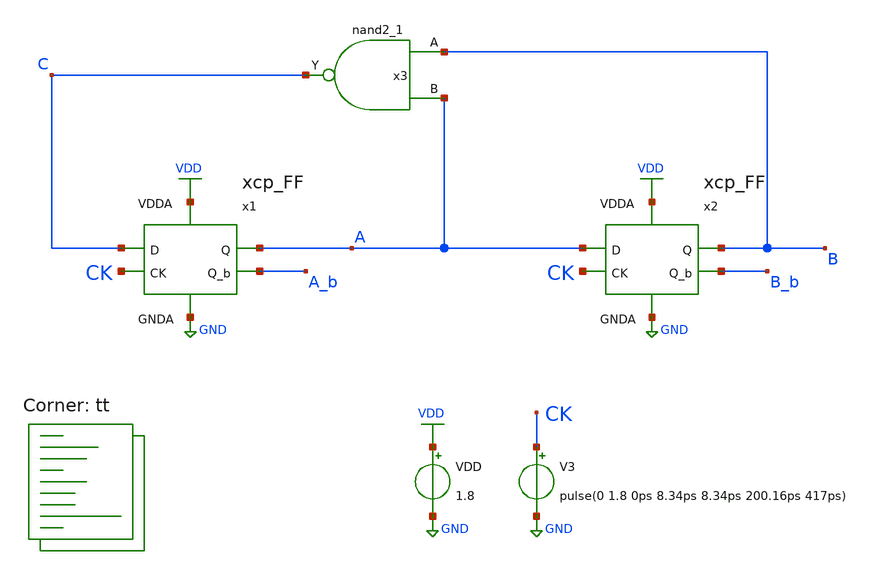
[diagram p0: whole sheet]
** sch_path: projects/pll/divider/xschem_ngspice/tb_xcp_FF_divide3.sch
**.subckt tb_xcp_FF_divide3
VDD VDD GND 1.8
V3 CK GND pulse(0 1.8 0ps 8.34ps 8.34ps 200.16ps 417ps)
x1 VDD C A A_b CK GND xcp_FF
x2 VDD A B B_b CK GND xcp_FF
x3 B A VGND VNB VPB VPWR C sky130_fd_sc_hd__nand2_1
**** begin user architecture code



.include /foss/pdks/sky130A/libs.ref/sky130_fd_sc_hd/spice/sky130_fd_sc_hd.spice

.option method=gear
.option wnflag=1
* .option savecurrents

.save @m.x1.xm1.msky130_fd_pr__nfet_01v8[gm] @m.x1.xm2.msky130_fd_pr__nfet_01v8[gm] @m.x1.xm3.msky130_fd_pr__pfet_01v8[gm] @m.x1.xm4.msky130_fd_pr__pfet_01v8[gm] @m.x1.xm5.msky130_fd_pr__nfet_01v8[gm] @m.x2.xm1.msky130_fd_pr__nfet_01v8[gm] @m.x2.xm2.msky130_fd_pr__nfet_01v8[gm] @m.x2.xm3.msky130_fd_pr__pfet_01v8[gm] @m.x2.xm4.msky130_fd_pr__pfet_01v8[gm] @m.x2.xm5.msky130_fd_pr__nfet_01v8[gm] @v.x1.vmeas @v.x1.vmeas1 @v.x1.vmeas2 @v.x5.vmeas @v.x5.vmeas1 @v.x5.vmeas2


*.ic v(b)=0

.control

  save v(a) v(a_b) v(b) v(b_b) v(c) v(ck)
  * save all
  *tran 0.1n 1u
  tran 0.2p 10n
  *ac dec 20 1 1T
  remzerovec
  write tb_xcp_FF_divide3.raw
  set appendwrite

.endc



.lib $::SKYWATER_MODELS/sky130.lib.spice tt
**** end user architecture code
**.ends

* expanding   symbol:  /foss/designs/my_design/projects/pll/divider/xschem_ngspice/xcp_FF.sym # of
*+ pins=6
** sym_path: projects/pll/divider/xschem_ngspice/xcp_FF.sym
** sch_path: projects/pll/divider/xschem_ngspice/xcp_FF.sch
.subckt xcp_FF VDDA D Q Q_b CK GNDA
*.ipin VDDA
*.opin Q
*.ipin CK
*.ipin GNDA
*.ipin D
*.opin Q_b
x1 VDDA A_b A net2 net3 CK GNDA xcp_latch
x2 VDDA Q_b Q A_b A net1 GNDA xcp_latch
XM1 net1 CK GNDA GNDA sky130_fd_pr__nfet_01v8 L=0.15 W=1 nf=1 ad='int((nf+1)/2) * W/nf * 0.29' as='int((nf+2)/2) * W/nf * 0.29'
+ pd='2*int((nf+1)/2) * (W/nf + 0.29)' ps='2*int((nf+2)/2) * (W/nf + 0.29)' nrd='0.29 / W' nrs='0.29 / W'
+ sa=0 sb=0 sd=0 mult=1 m=1
XM2 net1 CK VDDA VDDA sky130_fd_pr__pfet_01v8 L=0.15 W=1 nf=1 ad='int((nf+1)/2) * W/nf * 0.29' as='int((nf+2)/2) * W/nf * 0.29'
+ pd='2*int((nf+1)/2) * (W/nf + 0.29)' ps='2*int((nf+2)/2) * (W/nf + 0.29)' nrd='0.29 / W' nrs='0.29 / W'
+ sa=0 sb=0 sd=0 mult=1 m=1
XM3 net2 D GNDA GNDA sky130_fd_pr__nfet_01v8 L=0.15 W=1 nf=1 ad='int((nf+1)/2) * W/nf * 0.29' as='int((nf+2)/2) * W/nf * 0.29'
+ pd='2*int((nf+1)/2) * (W/nf + 0.29)' ps='2*int((nf+2)/2) * (W/nf + 0.29)' nrd='0.29 / W' nrs='0.29 / W'
+ sa=0 sb=0 sd=0 mult=1 m=1
XM4 net2 D GNDA GNDA sky130_fd_pr__pfet_01v8 L=0.15 W=1 nf=1 ad='int((nf+1)/2) * W/nf * 0.29' as='int((nf+2)/2) * W/nf * 0.29'
+ pd='2*int((nf+1)/2) * (W/nf + 0.29)' ps='2*int((nf+2)/2) * (W/nf + 0.29)' nrd='0.29 / W' nrs='0.29 / W'
+ sa=0 sb=0 sd=0 mult=1 m=1
XM5 net3 GNDA D VDDA sky130_fd_pr__pfet_01v8 L=0.15 W=1 nf=1 ad='int((nf+1)/2) * W/nf * 0.29' as='int((nf+2)/2) * W/nf * 0.29'
+ pd='2*int((nf+1)/2) * (W/nf + 0.29)' ps='2*int((nf+2)/2) * (W/nf + 0.29)' nrd='0.29 / W' nrs='0.29 / W'
+ sa=0 sb=0 sd=0 mult=1 m=1
XM6 net3 VDDA D GNDA sky130_fd_pr__nfet_01v8 L=0.15 W=1 nf=1 ad='int((nf+1)/2) * W/nf * 0.29' as='int((nf+2)/2) * W/nf * 0.29'
+ pd='2*int((nf+1)/2) * (W/nf + 0.29)' ps='2*int((nf+2)/2) * (W/nf + 0.29)' nrd='0.29 / W' nrs='0.29 / W'
+ sa=0 sb=0 sd=0 mult=1 m=1
.ends


* expanding   symbol:  /foss/designs/my_design/projects/pll/divider/xschem_ngspice/xcp_latch.sym #
*+ of pins=7
** sym_path: projects/pll/divider/xschem_ngspice/xcp_latch.sym
** sch_path: projects/pll/divider/xschem_ngspice/xcp_latch.sch
.subckt xcp_latch VDDA Q_b Q D_b D CK GNDA
*.ipin D
*.opin Q
*.ipin D_b
*.ipin CK
*.opin Q_b
*.ipin VDDA
*.ipin GNDA
XM5 net1 CK GNDA GNDA sky130_fd_pr__nfet_01v8 L=0.15 W=2 nf=2 ad='int((nf+1)/2) * W/nf * 0.29' as='int((nf+2)/2) * W/nf * 0.29'
+ pd='2*int((nf+1)/2) * (W/nf + 0.29)' ps='2*int((nf+2)/2) * (W/nf + 0.29)' nrd='0.29 / W' nrs='0.29 / W'
+ sa=0 sb=0 sd=0 mult=1 m=1
XM1 net3 D V_common GNDA sky130_fd_pr__nfet_01v8 L=0.15 W=1 nf=1 ad='int((nf+1)/2) * W/nf * 0.29' as='int((nf+2)/2) * W/nf * 0.29'
+ pd='2*int((nf+1)/2) * (W/nf + 0.29)' ps='2*int((nf+2)/2) * (W/nf + 0.29)' nrd='0.29 / W' nrs='0.29 / W'
+ sa=0 sb=0 sd=0 mult=1 m=1
XM2 net2 D_b V_common GNDA sky130_fd_pr__nfet_01v8 L=0.15 W=1 nf=1 ad='int((nf+1)/2) * W/nf * 0.29' as='int((nf+2)/2) * W/nf * 0.29'
+ pd='2*int((nf+1)/2) * (W/nf + 0.29)' ps='2*int((nf+2)/2) * (W/nf + 0.29)' nrd='0.29 / W' nrs='0.29 / W'
+ sa=0 sb=0 sd=0 mult=1 m=1
Vmeas V_common net1 0
.save i(vmeas)
Vmeas1 Q_b net3 0
.save i(vmeas1)
Vmeas2 Q net2 0
.save i(vmeas2)
XM3 Q_b Q VDDA VDDA sky130_fd_pr__pfet_01v8 L=0.15 W=1 nf=1 ad='int((nf+1)/2) * W/nf * 0.29' as='int((nf+2)/2) * W/nf * 0.29'
+ pd='2*int((nf+1)/2) * (W/nf + 0.29)' ps='2*int((nf+2)/2) * (W/nf + 0.29)' nrd='0.29 / W' nrs='0.29 / W'
+ sa=0 sb=0 sd=0 mult=1 m=1
XM4 Q Q_b VDDA VDDA sky130_fd_pr__pfet_01v8 L=0.15 W=1 nf=1 ad='int((nf+1)/2) * W/nf * 0.29' as='int((nf+2)/2) * W/nf * 0.29'
+ pd='2*int((nf+1)/2) * (W/nf + 0.29)' ps='2*int((nf+2)/2) * (W/nf + 0.29)' nrd='0.29 / W' nrs='0.29 / W'
+ sa=0 sb=0 sd=0 mult=1 m=1
.ends

.GLOBAL GND
.GLOBAL VDD
.end
